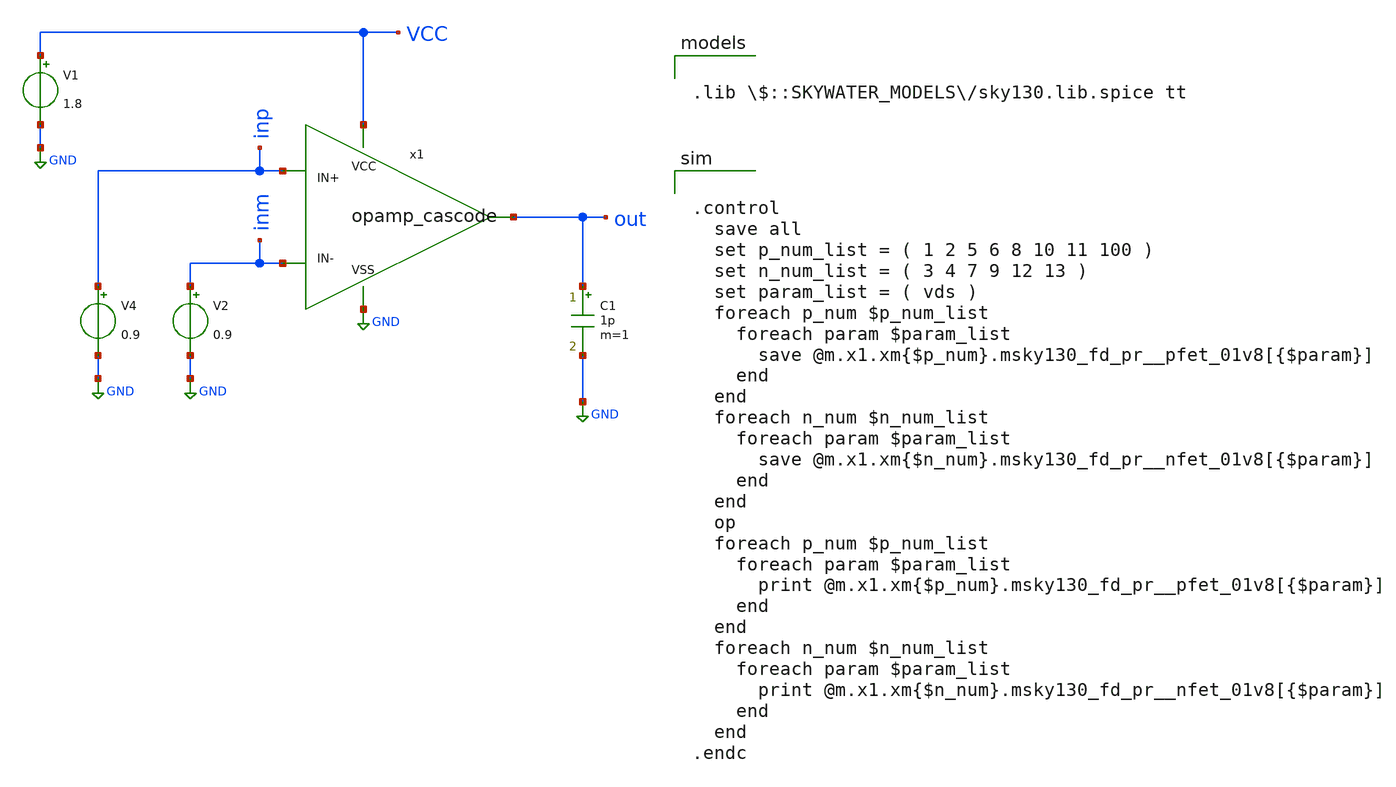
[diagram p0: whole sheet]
** sch_path: opamp_cascode_op_point.sch
**.subckt opamp_cascode_op_point
V1 VCC GND 1.8
V4 inp GND 0.9
V2 inm GND 0.9
C1 out GND 1p m=1
x1 VCC GND inp inm out opamp_cascode
**** begin user architecture code


.control
  save all
  set p_num_list = ( 1 2 5 6 8 10 11 100 )
  set n_num_list = ( 3 4 7 9 12 13 )
  set param_list = ( vds )
  foreach p_num $p_num_list
    foreach param $param_list
      save @m.x1.xm{$p_num}.msky130_fd_pr__pfet_01v8[{$param}]
    end
  end
  foreach n_num $n_num_list
    foreach param $param_list
      save @m.x1.xm{$n_num}.msky130_fd_pr__nfet_01v8[{$param}]
    end
  end
  op
  foreach p_num $p_num_list
    foreach param $param_list
      print @m.x1.xm{$p_num}.msky130_fd_pr__pfet_01v8[{$param}]
    end
  end
  foreach n_num $n_num_list
    foreach param $param_list
      print @m.x1.xm{$n_num}.msky130_fd_pr__nfet_01v8[{$param}]
    end
  end
.endc



.lib $::SKYWATER_MODELS/sky130.lib.spice tt

**** end user architecture code
**.ends

* expanding   symbol:  /home/zwierzak/projects/SKY130_OpAmp_GIT/opamp_cascode.sym # of pins=5
** sym_path: opamp_cascode.sym
** sch_path: opamp_cascode.sch
.subckt opamp_cascode VCC VSS IN+ IN- OUT
*.ipin IN+
*.ipin IN-
*.ipin VCC
*.ipin VSS
*.opin OUT
XM10 net8 net6 VCC VCC sky130_fd_pr__pfet_01v8 L=10 W=40 nf=1 ad='int((nf+1)/2) * W/nf * 0.29' as='int((nf+2)/2) * W/nf * 0.29'
+ pd='2*int((nf+1)/2) * (W/nf + 0.29)' ps='2*int((nf+2)/2) * (W/nf + 0.29)' nrd='0.29 / W' nrs='0.29 / W'
+ sa=0 sb=0 sd=0 mult=2 m=2
XM1 net7 net6 VCC VCC sky130_fd_pr__pfet_01v8 L=10 W=40 nf=1 ad='int((nf+1)/2) * W/nf * 0.29' as='int((nf+2)/2) * W/nf * 0.29'
+ pd='2*int((nf+1)/2) * (W/nf + 0.29)' ps='2*int((nf+2)/2) * (W/nf + 0.29)' nrd='0.29 / W' nrs='0.29 / W'
+ sa=0 sb=0 sd=0 mult=2 m=2
XM5 net3 net9 VCC VCC sky130_fd_pr__pfet_01v8 L=3 W=20 nf=1 ad='int((nf+1)/2) * W/nf * 0.29' as='int((nf+2)/2) * W/nf * 0.29'
+ pd='2*int((nf+1)/2) * (W/nf + 0.29)' ps='2*int((nf+2)/2) * (W/nf + 0.29)' nrd='0.29 / W' nrs='0.29 / W'
+ sa=0 sb=0 sd=0 mult=10 m=10
XM100 net9 net9 VCC VCC sky130_fd_pr__pfet_01v8 L=3 W=20 nf=1 ad='int((nf+1)/2) * W/nf * 0.29' as='int((nf+2)/2) * W/nf * 0.29'
+ pd='2*int((nf+1)/2) * (W/nf + 0.29)' ps='2*int((nf+2)/2) * (W/nf + 0.29)' nrd='0.29 / W' nrs='0.29 / W'
+ sa=0 sb=0 sd=0 mult=1 m=1
I0 net9 VSS 3.5u
XM11 OUT BIAS net8 net8 sky130_fd_pr__pfet_01v8 L=3 W=20 nf=1 ad='int((nf+1)/2) * W/nf * 0.29' as='int((nf+2)/2) * W/nf * 0.29'
+ pd='2*int((nf+1)/2) * (W/nf + 0.29)' ps='2*int((nf+2)/2) * (W/nf + 0.29)' nrd='0.29 / W' nrs='0.29 / W'
+ sa=0 sb=0 sd=0 mult=10 m=10
XM2 net6 BIAS net7 net7 sky130_fd_pr__pfet_01v8 L=3 W=20 nf=1 ad='int((nf+1)/2) * W/nf * 0.29' as='int((nf+2)/2) * W/nf * 0.29'
+ pd='2*int((nf+1)/2) * (W/nf + 0.29)' ps='2*int((nf+2)/2) * (W/nf + 0.29)' nrd='0.29 / W' nrs='0.29 / W'
+ sa=0 sb=0 sd=0 mult=10 m=10
XM6 net1 IN- net3 net3 sky130_fd_pr__pfet_01v8 L=0.25 W=25 nf=2 ad='int((nf+1)/2) * W/nf * 0.29' as='int((nf+2)/2) * W/nf * 0.29'
+ pd='2*int((nf+1)/2) * (W/nf + 0.29)' ps='2*int((nf+2)/2) * (W/nf + 0.29)' nrd='0.29 / W' nrs='0.29 / W'
+ sa=0 sb=0 sd=0 mult=3 m=3
XM8 net2 IN+ net3 net3 sky130_fd_pr__pfet_01v8 L=0.25 W=25 nf=2 ad='int((nf+1)/2) * W/nf * 0.29' as='int((nf+2)/2) * W/nf * 0.29'
+ pd='2*int((nf+1)/2) * (W/nf + 0.29)' ps='2*int((nf+2)/2) * (W/nf + 0.29)' nrd='0.29 / W' nrs='0.29 / W'
+ sa=0 sb=0 sd=0 mult=3 m=3
XM7 net1 net1 VSS VSS sky130_fd_pr__nfet_01v8 L=10 W=20 nf=1 ad='int((nf+1)/2) * W/nf * 0.29' as='int((nf+2)/2) * W/nf * 0.29'
+ pd='2*int((nf+1)/2) * (W/nf + 0.29)' ps='2*int((nf+2)/2) * (W/nf + 0.29)' nrd='0.29 / W' nrs='0.29 / W'
+ sa=0 sb=0 sd=0 mult=1 m=1
XM9 net2 net2 VSS VSS sky130_fd_pr__nfet_01v8 L=10 W=20 nf=1 ad='int((nf+1)/2) * W/nf * 0.29' as='int((nf+2)/2) * W/nf * 0.29'
+ pd='2*int((nf+1)/2) * (W/nf + 0.29)' ps='2*int((nf+2)/2) * (W/nf + 0.29)' nrd='0.29 / W' nrs='0.29 / W'
+ sa=0 sb=0 sd=0 mult=1 m=1
XM13 net4 net2 VSS VSS sky130_fd_pr__nfet_01v8 L=10 W=20 nf=1 ad='int((nf+1)/2) * W/nf * 0.29' as='int((nf+2)/2) * W/nf * 0.29'
+ pd='2*int((nf+1)/2) * (W/nf + 0.29)' ps='2*int((nf+2)/2) * (W/nf + 0.29)' nrd='0.29 / W' nrs='0.29 / W'
+ sa=0 sb=0 sd=0 mult=3 m=3
XM4 net5 net1 VSS VSS sky130_fd_pr__nfet_01v8 L=10 W=20 nf=1 ad='int((nf+1)/2) * W/nf * 0.29' as='int((nf+2)/2) * W/nf * 0.29'
+ pd='2*int((nf+1)/2) * (W/nf + 0.29)' ps='2*int((nf+2)/2) * (W/nf + 0.29)' nrd='0.29 / W' nrs='0.29 / W'
+ sa=0 sb=0 sd=0 mult=3 m=3
XM12 OUT BIAS1 net4 net4 sky130_fd_pr__nfet_01v8 L=3 W=20 nf=1 ad='int((nf+1)/2) * W/nf * 0.29' as='int((nf+2)/2) * W/nf * 0.29'
+ pd='2*int((nf+1)/2) * (W/nf + 0.29)' ps='2*int((nf+2)/2) * (W/nf + 0.29)' nrd='0.29 / W' nrs='0.29 / W'
+ sa=0 sb=0 sd=0 mult=5 m=5
XM3 net6 BIAS1 net5 net5 sky130_fd_pr__nfet_01v8 L=3 W=20 nf=1 ad='int((nf+1)/2) * W/nf * 0.29' as='int((nf+2)/2) * W/nf * 0.29'
+ pd='2*int((nf+1)/2) * (W/nf + 0.29)' ps='2*int((nf+2)/2) * (W/nf + 0.29)' nrd='0.29 / W' nrs='0.29 / W'
+ sa=0 sb=0 sd=0 mult=5 m=5
V1 BIAS VSS 0
V2 BIAS1 VSS 0.6
.ends

.GLOBAL GND
.end
